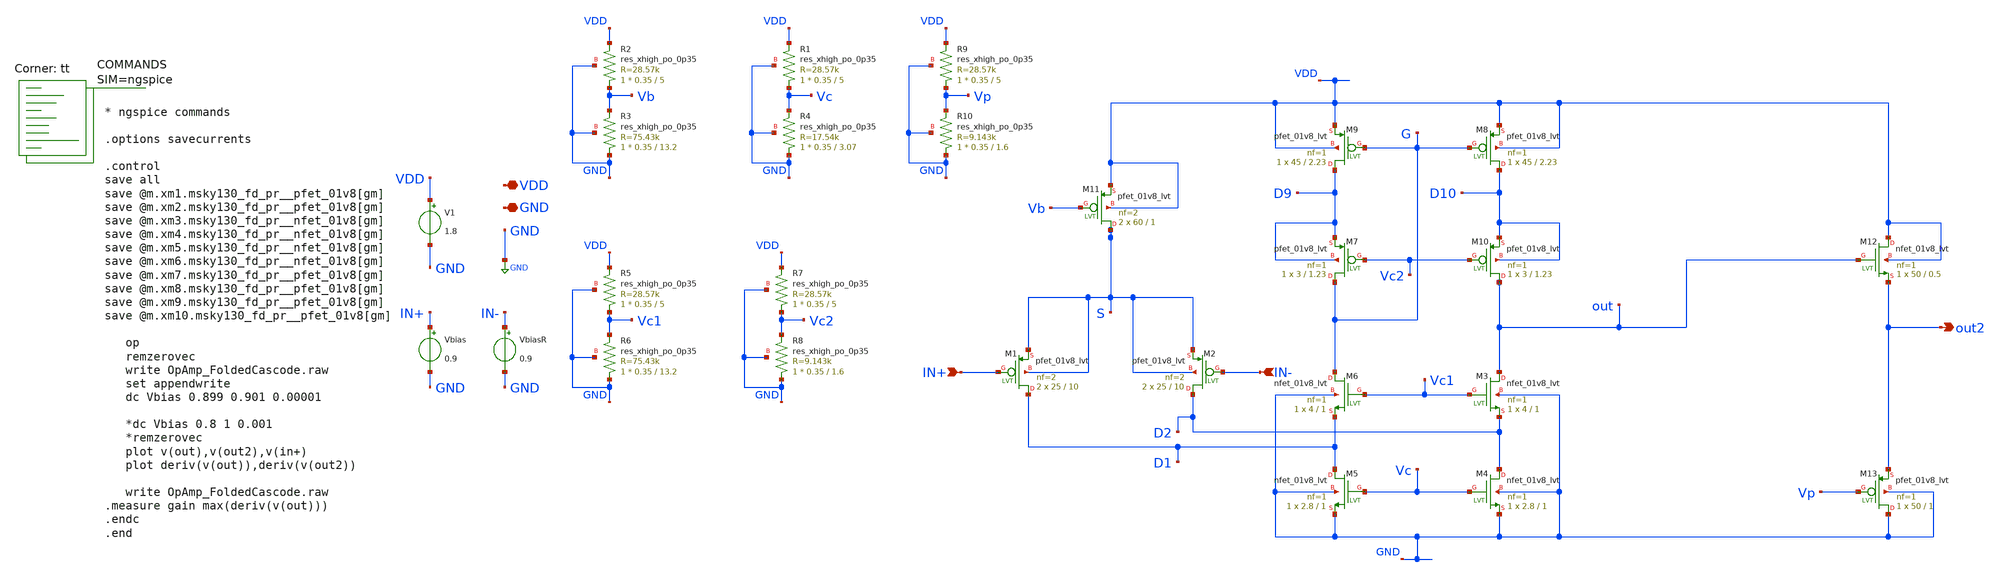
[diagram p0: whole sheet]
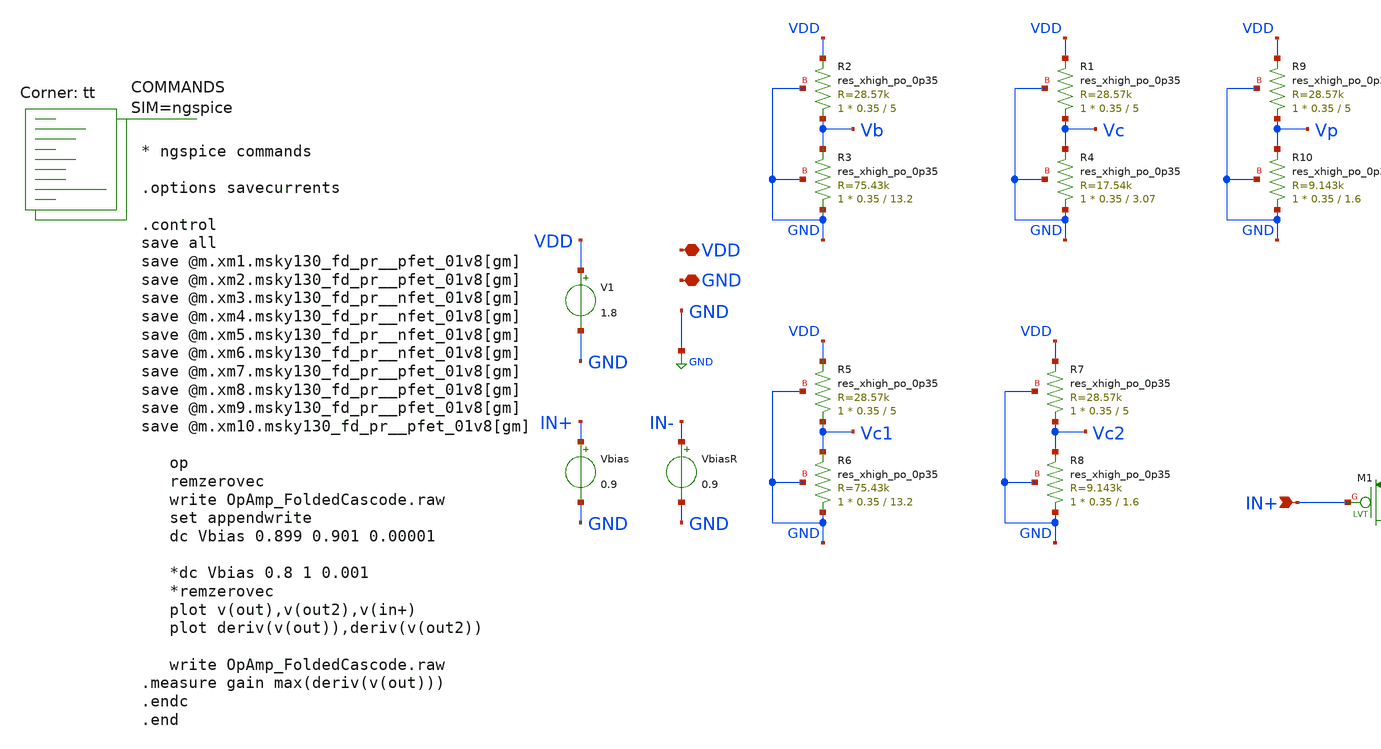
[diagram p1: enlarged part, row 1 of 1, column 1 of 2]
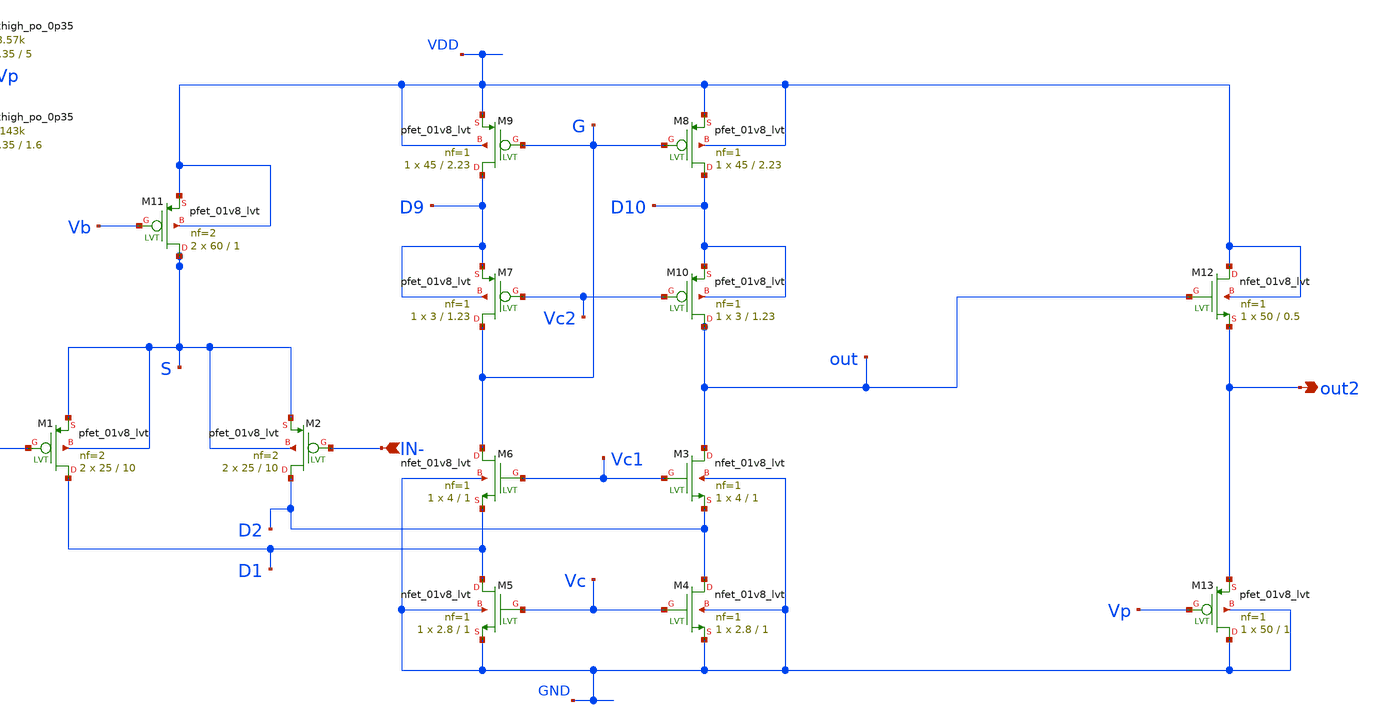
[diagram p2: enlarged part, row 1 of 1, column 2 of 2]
** sch_path: xschem/OpAmp_FoldedCascode.sch
**.subckt OpAmp_FoldedCascode out2 VDD GND IN+ IN-
*.opin out2
*.iopin VDD
*.iopin GND
*.ipin IN+
*.ipin IN-
V1 VDD GND 1.8
Vbias IN+ GND 0.9
VbiasR IN- GND 0.9
XR2 Vb VDD GND sky130_fd_pr__res_xhigh_po_0p35 L=5 mult=1 m=1
XR3 GND Vb GND sky130_fd_pr__res_xhigh_po_0p35 L=13.2 mult=1 m=1
XR1 Vc VDD GND sky130_fd_pr__res_xhigh_po_0p35 L=5 mult=1 m=1
XR4 GND Vc GND sky130_fd_pr__res_xhigh_po_0p35 L=3.07 mult=1 m=1
XR5 Vc1 VDD GND sky130_fd_pr__res_xhigh_po_0p35 L=5 mult=1 m=1
XR6 GND Vc1 GND sky130_fd_pr__res_xhigh_po_0p35 L=13.2 mult=1 m=1
XR7 Vc2 VDD GND sky130_fd_pr__res_xhigh_po_0p35 L=5 mult=1 m=1
XR8 GND Vc2 GND sky130_fd_pr__res_xhigh_po_0p35 L=1.6 mult=1 m=1
XM11 S Vb VDD VDD sky130_fd_pr__pfet_01v8_lvt L=1 W=60 nf=2 ad='int((nf+1)/2) * W/nf * 0.29' as='int((nf+2)/2) * W/nf * 0.29'
+ pd='2*int((nf+1)/2) * (W/nf + 0.29)' ps='2*int((nf+2)/2) * (W/nf + 0.29)' nrd='0.29 / W' nrs='0.29 / W'
+ sa=0 sb=0 sd=0 mult=2 m=2
XM1 D1 IN+ S S sky130_fd_pr__pfet_01v8_lvt L=10 W=25 nf=2 ad='int((nf+1)/2) * W/nf * 0.29' as='int((nf+2)/2) * W/nf * 0.29'
+ pd='2*int((nf+1)/2) * (W/nf + 0.29)' ps='2*int((nf+2)/2) * (W/nf + 0.29)' nrd='0.29 / W' nrs='0.29 / W'
+ sa=0 sb=0 sd=0 mult=2 m=2
XM2 D2 IN- S S sky130_fd_pr__pfet_01v8_lvt L=10 W=25 nf=2 ad='int((nf+1)/2) * W/nf * 0.29' as='int((nf+2)/2) * W/nf * 0.29'
+ pd='2*int((nf+1)/2) * (W/nf + 0.29)' ps='2*int((nf+2)/2) * (W/nf + 0.29)' nrd='0.29 / W' nrs='0.29 / W'
+ sa=0 sb=0 sd=0 mult=2 m=2
XM3 out Vc1 D2 GND sky130_fd_pr__nfet_01v8_lvt L=1 W=4 nf=1 ad='int((nf+1)/2) * W/nf * 0.29' as='int((nf+2)/2) * W/nf * 0.29'
+ pd='2*int((nf+1)/2) * (W/nf + 0.29)' ps='2*int((nf+2)/2) * (W/nf + 0.29)' nrd='0.29 / W' nrs='0.29 / W'
+ sa=0 sb=0 sd=0 mult=1 m=1
XM4 D2 Vc GND GND sky130_fd_pr__nfet_01v8_lvt L=1 W=2.8 nf=1 ad='int((nf+1)/2) * W/nf * 0.29' as='int((nf+2)/2) * W/nf * 0.29'
+ pd='2*int((nf+1)/2) * (W/nf + 0.29)' ps='2*int((nf+2)/2) * (W/nf + 0.29)' nrd='0.29 / W' nrs='0.29 / W'
+ sa=0 sb=0 sd=0 mult=1 m=1
XM5 D1 Vc GND GND sky130_fd_pr__nfet_01v8_lvt L=1 W=2.8 nf=1 ad='int((nf+1)/2) * W/nf * 0.29' as='int((nf+2)/2) * W/nf * 0.29'
+ pd='2*int((nf+1)/2) * (W/nf + 0.29)' ps='2*int((nf+2)/2) * (W/nf + 0.29)' nrd='0.29 / W' nrs='0.29 / W'
+ sa=0 sb=0 sd=0 mult=1 m=1
XM6 G Vc1 D1 GND sky130_fd_pr__nfet_01v8_lvt L=1 W=4 nf=1 ad='int((nf+1)/2) * W/nf * 0.29' as='int((nf+2)/2) * W/nf * 0.29'
+ pd='2*int((nf+1)/2) * (W/nf + 0.29)' ps='2*int((nf+2)/2) * (W/nf + 0.29)' nrd='0.29 / W' nrs='0.29 / W'
+ sa=0 sb=0 sd=0 mult=1 m=1
XM7 G Vc2 D9 D9 sky130_fd_pr__pfet_01v8_lvt L=1.23 W=3 nf=1 ad='int((nf+1)/2) * W/nf * 0.29' as='int((nf+2)/2) * W/nf * 0.29'
+ pd='2*int((nf+1)/2) * (W/nf + 0.29)' ps='2*int((nf+2)/2) * (W/nf + 0.29)' nrd='0.29 / W' nrs='0.29 / W'
+ sa=0 sb=0 sd=0 mult=1 m=1
XM9 D9 G VDD VDD sky130_fd_pr__pfet_01v8_lvt L=2.23 W=45 nf=1 ad='int((nf+1)/2) * W/nf * 0.29' as='int((nf+2)/2) * W/nf * 0.29'
+ pd='2*int((nf+1)/2) * (W/nf + 0.29)' ps='2*int((nf+2)/2) * (W/nf + 0.29)' nrd='0.29 / W' nrs='0.29 / W'
+ sa=0 sb=0 sd=0 mult=1 m=1
XM8 D10 G VDD VDD sky130_fd_pr__pfet_01v8_lvt L=2.23 W=45 nf=1 ad='int((nf+1)/2) * W/nf * 0.29' as='int((nf+2)/2) * W/nf * 0.29'
+ pd='2*int((nf+1)/2) * (W/nf + 0.29)' ps='2*int((nf+2)/2) * (W/nf + 0.29)' nrd='0.29 / W' nrs='0.29 / W'
+ sa=0 sb=0 sd=0 mult=1 m=1
XM10 out Vc2 D10 D10 sky130_fd_pr__pfet_01v8_lvt L=1.23 W=3 nf=1 ad='int((nf+1)/2) * W/nf * 0.29' as='int((nf+2)/2) * W/nf * 0.29'
+ pd='2*int((nf+1)/2) * (W/nf + 0.29)' ps='2*int((nf+2)/2) * (W/nf + 0.29)' nrd='0.29 / W' nrs='0.29 / W'
+ sa=0 sb=0 sd=0 mult=1 m=1
XR9 Vp VDD GND sky130_fd_pr__res_xhigh_po_0p35 L=5 mult=1 m=1
XR10 GND Vp GND sky130_fd_pr__res_xhigh_po_0p35 L=1.6 mult=1 m=1
XM12 VDD out out2 VDD sky130_fd_pr__nfet_01v8_lvt L=0.5 W=50 nf=1 ad='int((nf+1)/2) * W/nf * 0.29' as='int((nf+2)/2) * W/nf * 0.29'
+ pd='2*int((nf+1)/2) * (W/nf + 0.29)' ps='2*int((nf+2)/2) * (W/nf + 0.29)' nrd='0.29 / W' nrs='0.29 / W'
+ sa=0 sb=0 sd=0 mult=1 m=1
XM13 GND Vp out2 GND sky130_fd_pr__pfet_01v8_lvt L=1 W=50 nf=1 ad='int((nf+1)/2) * W/nf * 0.29' as='int((nf+2)/2) * W/nf * 0.29'
+ pd='2*int((nf+1)/2) * (W/nf + 0.29)' ps='2*int((nf+2)/2) * (W/nf + 0.29)' nrd='0.29 / W' nrs='0.29 / W'
+ sa=0 sb=0 sd=0 mult=1 m=1
**** begin user architecture code



* ngspice commands

.options savecurrents

.control
save all
save @m.xm1.msky130_fd_pr__pfet_01v8[gm]
save @m.xm2.msky130_fd_pr__pfet_01v8[gm]
save @m.xm3.msky130_fd_pr__nfet_01v8[gm]
save @m.xm4.msky130_fd_pr__nfet_01v8[gm]
save @m.xm5.msky130_fd_pr__nfet_01v8[gm]
save @m.xm6.msky130_fd_pr__nfet_01v8[gm]
save @m.xm7.msky130_fd_pr__pfet_01v8[gm]
save @m.xm8.msky130_fd_pr__pfet_01v8[gm]
save @m.xm9.msky130_fd_pr__pfet_01v8[gm]
save @m.xm10.msky130_fd_pr__pfet_01v8[gm]

   op
   remzerovec
   write OpAmp_FoldedCascode.raw
   set appendwrite
   dc Vbias 0.899 0.901 0.00001

   *dc Vbias 0.8 1 0.001
   *remzerovec
   plot v(out),v(out2),v(in+)
   plot deriv(v(out)),deriv(v(out2))

   write OpAmp_FoldedCascode.raw
.measure gain max(deriv(v(out)))
.endc
.end



.lib $::SKYWATER_MODELS/sky130.lib.spice tt
**** end user architecture code
**.ends
.GLOBAL GND
.end
